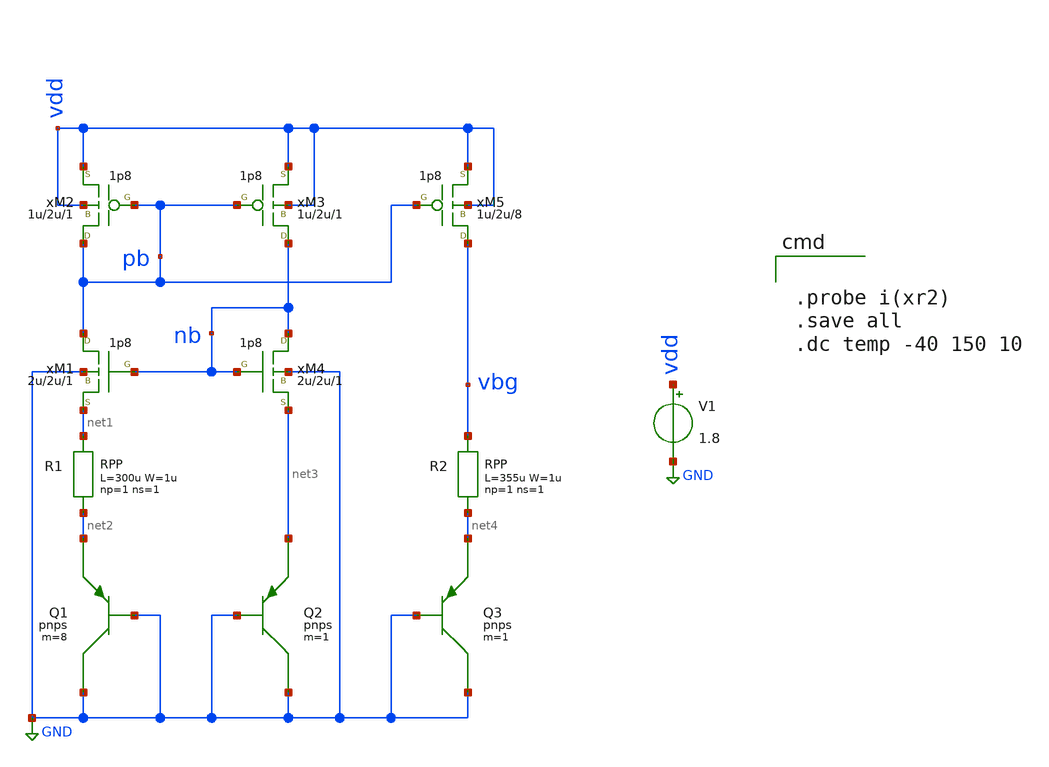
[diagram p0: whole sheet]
** sch_path: xschem/gen18_examples/bg.sch
**.subckt bg
V1 vdd GND 1.8
xR2 vbg net4 RPP W=1u L=355u np=1 ns=1
xR1 net1 net2 RPP W=1u L=300u np=1 ns=1
xM1 pb nb net1 GND nmos18 w=2u l=2u m=1
xM4 nb nb net3 GND nmos18 w=2u l=2u m=1
xM2 pb pb vdd vdd pmos18 w=1u l=2u m=1
xM3 nb pb vdd vdd pmos18 w=1u l=2u m=1
xM5 vbg pb vdd vdd pmos18 w=1u l=2u m=8
xQ1 GND GND net2 pnps m=8
xQ2 GND GND net3 pnps m=1
xQ3 GND GND net4 pnps m=1
**** begin user architecture code

.probe i(xr2)
.save all
.dc temp -40 150 10

.include  [path_head [abs_sym_path gen18/gen18models.sym] 3]/mdl/gen18.inc
**** end user architecture code
**.ends
.GLOBAL GND
.end
